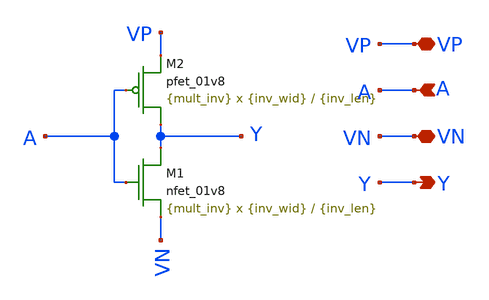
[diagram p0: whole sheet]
** sch_path: Circuits, Symbols, Extras/inverter.sch
**.subckt inverter VP A Y VN
*.iopin VP
*.ipin A
*.opin Y
*.iopin VN
XM2 Y A VP VP sky130_fd_pr__pfet_01v8 L={inv_len} W={inv_wid} nf=1 ad='int((nf+1)/2) * W/nf * 0.29' as='int((nf+2)/2) * W/nf * 0.29'
+ pd='2*int((nf+1)/2) * (W/nf + 0.29)' ps='2*int((nf+2)/2) * (W/nf + 0.29)' nrd='0.29 / W' nrs='0.29 / W'
+ sa=0 sb=0 sd=0 mult={mult_inv} m={mult_inv}
XM1 Y A VN VN sky130_fd_pr__nfet_01v8 L={inv_len} W={inv_wid} nf=1 ad='int((nf+1)/2) * W/nf * 0.29' as='int((nf+2)/2) * W/nf * 0.29'
+ pd='2*int((nf+1)/2) * (W/nf + 0.29)' ps='2*int((nf+2)/2) * (W/nf + 0.29)' nrd='0.29 / W' nrs='0.29 / W'
+ sa=0 sb=0 sd=0 mult={mult_inv} m={mult_inv}
**.ends
.end
